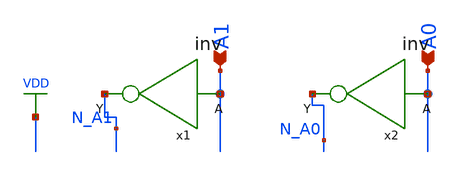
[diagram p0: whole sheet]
** sch_path: circuits/xschem/partials/pmos_header.sch
**.subckt pmos_header A1 A0
*.ipin A1
*.ipin A0
x1 N_A1 A1 inv
x2 N_A0 A0 inv
**.ends

* expanding   symbol:  lab1/inv.sym # of pins=2
** sym_path: library/xschem/lab1/inv.sym
** sch_path: library/xschem/lab1/inv.sch
.subckt inv Y A
*.ipin A
*.opin Y
XM1 Y A GND GND sky130_fd_pr__nfet_01v8 L=0.15 W=0.5 nf=1 ad='int((nf+1)/2) * W/nf * 0.29' as='int((nf+2)/2) * W/nf * 0.29'
+ pd='2*int((nf+1)/2) * (W/nf + 0.29)' ps='2*int((nf+2)/2) * (W/nf + 0.29)' nrd='0.29 / W' nrs='0.29 / W'
+ sa=0 sb=0 sd=0 mult=1 m=1
XM2 Y A VDD VDD sky130_fd_pr__pfet_01v8 L=0.15 W=1 nf=1 ad='int((nf+1)/2) * W/nf * 0.29' as='int((nf+2)/2) * W/nf * 0.29'
+ pd='2*int((nf+1)/2) * (W/nf + 0.29)' ps='2*int((nf+2)/2) * (W/nf + 0.29)' nrd='0.29 / W' nrs='0.29 / W'
+ sa=0 sb=0 sd=0 mult=1 m=1
.ends

.GLOBAL VDD
.GLOBAL GND
.end
